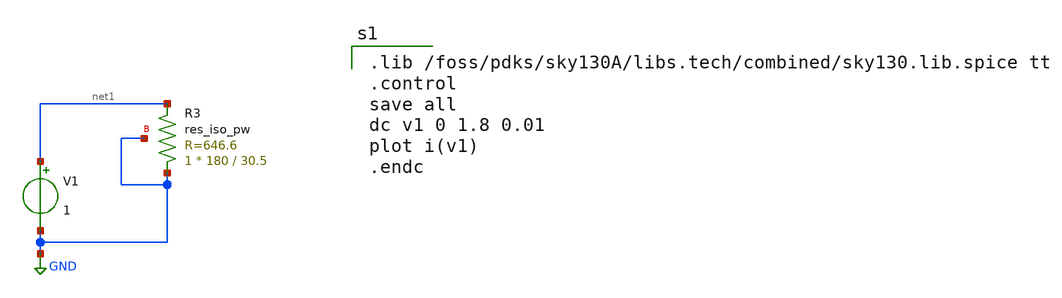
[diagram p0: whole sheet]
** sch_path: res_iso_corners.sch
**.subckt res_iso_corners
XR3 GND net1 GND sky130_fd_pr__res_iso_pw W=180 L=30.5 m=1
V1 net1 GND 1
**** begin user architecture code

.lib /foss/pdks/sky130A/libs.tech/combined/sky130.lib.spice tt
.control
save all
dc v1 0 1.8 0.01
plot i(v1)
.endc


**** end user architecture code
**.ends
.GLOBAL GND
.end
